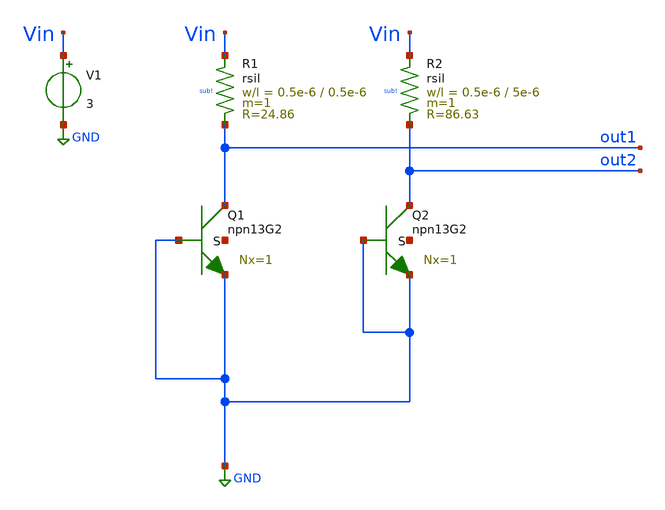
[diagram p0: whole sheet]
** sch_path: xschem/silicon-bandgap-temp-sensor.sch
**.subckt silicon-bandgap-temp-sensor
XQ1 out1 GND GND net1 npn13G2 Nx=1 mm_ok=1
XQ2 out2 GND GND net2 npn13G2 Nx=1 mm_ok=1
XR1 Vin out1 sub! rsil w=0.5e-6 l=0.5e-6 m=1 mm_ok=1
XR2 Vin out2 sub! rsil w=0.5e-6 l=5e-6 m=1 mm_ok=1
V1 Vin GND 3
**.ends
.GLOBAL GND
.end
